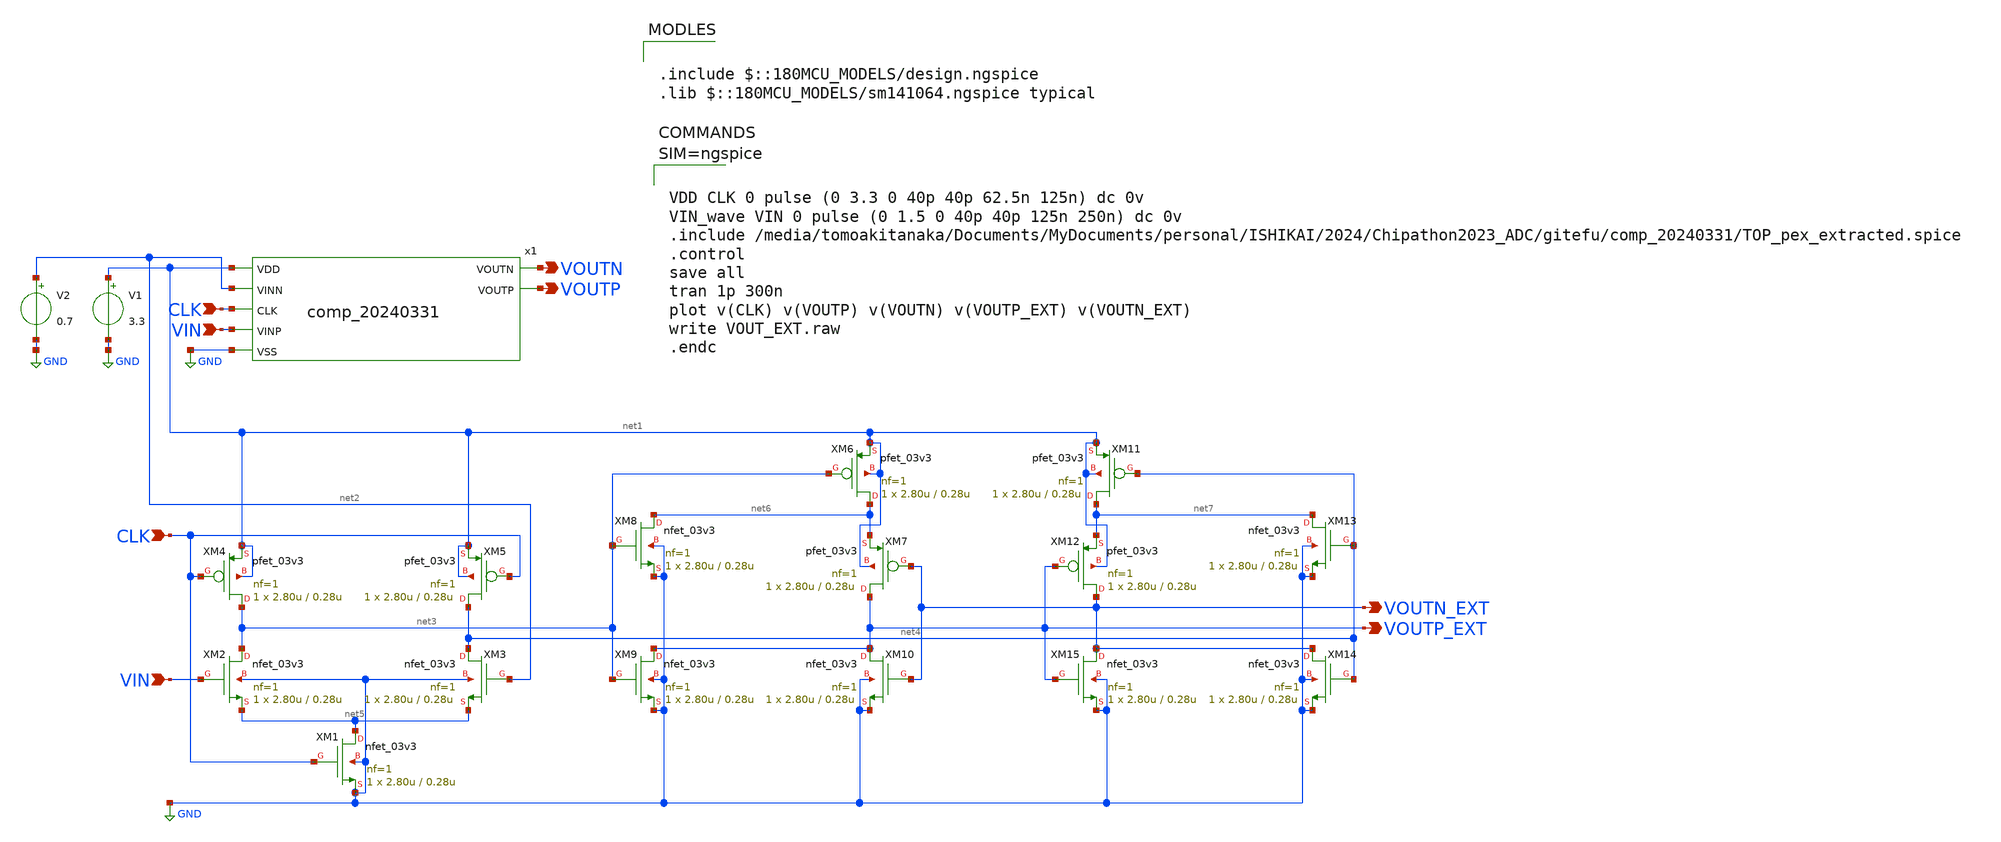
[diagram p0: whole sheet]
** sch_path: gitefu/tb/tb_check_pulse.sch
**.subckt tb_check_pulse CLK VOUTN VOUTP VIN CLK VIN VOUTP_EXT VOUTN_EXT
*.ipin CLK
*.opin VOUTN
*.opin VOUTP
*.ipin VIN
*.ipin CLK
*.ipin VIN
*.opin VOUTP_EXT
*.opin VOUTN_EXT
V1 net1 GND 3.3
V2 net2 GND 0.7
XM1 net5 CLK GND GND nfet_03v3 L=0.28u W=2.80u nf=1 ad='int((nf+1)/2) * W/nf * 0.18u' as='int((nf+2)/2) * W/nf * 0.18u'
+ pd='2*int((nf+1)/2) * (W/nf + 0.18u)' ps='2*int((nf+2)/2) * (W/nf + 0.18u)' nrd='0.18u / W' nrs='0.18u / W'
+ sa=0 sb=0 sd=0 m=1
XM2 net3 VIN net5 GND nfet_03v3 L=0.28u W=2.80u nf=1 ad='int((nf+1)/2) * W/nf * 0.18u' as='int((nf+2)/2) * W/nf * 0.18u'
+ pd='2*int((nf+1)/2) * (W/nf + 0.18u)' ps='2*int((nf+2)/2) * (W/nf + 0.18u)' nrd='0.18u / W' nrs='0.18u / W'
+ sa=0 sb=0 sd=0 m=1
XM4 net3 CLK net1 net1 pfet_03v3 L=0.28u W=2.80u nf=1 ad='int((nf+1)/2) * W/nf * 0.18u' as='int((nf+2)/2) * W/nf * 0.18u'
+ pd='2*int((nf+1)/2) * (W/nf + 0.18u)' ps='2*int((nf+2)/2) * (W/nf + 0.18u)' nrd='0.18u / W' nrs='0.18u / W'
+ sa=0 sb=0 sd=0 m=1
XM6 net6 net3 net1 net1 pfet_03v3 L=0.28u W=2.80u nf=1 ad='int((nf+1)/2) * W/nf * 0.18u' as='int((nf+2)/2) * W/nf * 0.18u'
+ pd='2*int((nf+1)/2) * (W/nf + 0.18u)' ps='2*int((nf+2)/2) * (W/nf + 0.18u)' nrd='0.18u / W' nrs='0.18u / W'
+ sa=0 sb=0 sd=0 m=1
XM7 VOUTP_EXT VOUTN_EXT net6 net1 pfet_03v3 L=0.28u W=2.80u nf=1 ad='int((nf+1)/2) * W/nf * 0.18u' as='int((nf+2)/2) * W/nf * 0.18u'
+ pd='2*int((nf+1)/2) * (W/nf + 0.18u)' ps='2*int((nf+2)/2) * (W/nf + 0.18u)' nrd='0.18u / W' nrs='0.18u / W'
+ sa=0 sb=0 sd=0 m=1
XM8 net6 net3 GND GND nfet_03v3 L=0.28u W=2.80u nf=1 ad='int((nf+1)/2) * W/nf * 0.18u' as='int((nf+2)/2) * W/nf * 0.18u'
+ pd='2*int((nf+1)/2) * (W/nf + 0.18u)' ps='2*int((nf+2)/2) * (W/nf + 0.18u)' nrd='0.18u / W' nrs='0.18u / W'
+ sa=0 sb=0 sd=0 m=1
XM9 VOUTP_EXT net3 GND GND nfet_03v3 L=0.28u W=2.80u nf=1 ad='int((nf+1)/2) * W/nf * 0.18u' as='int((nf+2)/2) * W/nf * 0.18u'
+ pd='2*int((nf+1)/2) * (W/nf + 0.18u)' ps='2*int((nf+2)/2) * (W/nf + 0.18u)' nrd='0.18u / W' nrs='0.18u / W'
+ sa=0 sb=0 sd=0 m=1
XM10 VOUTP_EXT VOUTN_EXT GND GND nfet_03v3 L=0.28u W=2.80u nf=1 ad='int((nf+1)/2) * W/nf * 0.18u' as='int((nf+2)/2) * W/nf * 0.18u'
+ pd='2*int((nf+1)/2) * (W/nf + 0.18u)' ps='2*int((nf+2)/2) * (W/nf + 0.18u)' nrd='0.18u / W' nrs='0.18u / W'
+ sa=0 sb=0 sd=0 m=1
XM3 net4 net2 net5 GND nfet_03v3 L=0.28u W=2.80u nf=1 ad='int((nf+1)/2) * W/nf * 0.18u' as='int((nf+2)/2) * W/nf * 0.18u'
+ pd='2*int((nf+1)/2) * (W/nf + 0.18u)' ps='2*int((nf+2)/2) * (W/nf + 0.18u)' nrd='0.18u / W' nrs='0.18u / W'
+ sa=0 sb=0 sd=0 m=1
XM5 net4 CLK net1 net1 pfet_03v3 L=0.28u W=2.80u nf=1 ad='int((nf+1)/2) * W/nf * 0.18u' as='int((nf+2)/2) * W/nf * 0.18u'
+ pd='2*int((nf+1)/2) * (W/nf + 0.18u)' ps='2*int((nf+2)/2) * (W/nf + 0.18u)' nrd='0.18u / W' nrs='0.18u / W'
+ sa=0 sb=0 sd=0 m=1
XM11 net7 net4 net1 net1 pfet_03v3 L=0.28u W=2.80u nf=1 ad='int((nf+1)/2) * W/nf * 0.18u' as='int((nf+2)/2) * W/nf * 0.18u'
+ pd='2*int((nf+1)/2) * (W/nf + 0.18u)' ps='2*int((nf+2)/2) * (W/nf + 0.18u)' nrd='0.18u / W' nrs='0.18u / W'
+ sa=0 sb=0 sd=0 m=1
XM12 VOUTN_EXT VOUTP_EXT net7 net1 pfet_03v3 L=0.28u W=2.80u nf=1 ad='int((nf+1)/2) * W/nf * 0.18u' as='int((nf+2)/2) * W/nf * 0.18u'
+ pd='2*int((nf+1)/2) * (W/nf + 0.18u)' ps='2*int((nf+2)/2) * (W/nf + 0.18u)' nrd='0.18u / W' nrs='0.18u / W'
+ sa=0 sb=0 sd=0 m=1
XM13 net7 net4 GND GND nfet_03v3 L=0.28u W=2.80u nf=1 ad='int((nf+1)/2) * W/nf * 0.18u' as='int((nf+2)/2) * W/nf * 0.18u'
+ pd='2*int((nf+1)/2) * (W/nf + 0.18u)' ps='2*int((nf+2)/2) * (W/nf + 0.18u)' nrd='0.18u / W' nrs='0.18u / W'
+ sa=0 sb=0 sd=0 m=1
XM14 VOUTN_EXT net4 GND GND nfet_03v3 L=0.28u W=2.80u nf=1 ad='int((nf+1)/2) * W/nf * 0.18u' as='int((nf+2)/2) * W/nf * 0.18u'
+ pd='2*int((nf+1)/2) * (W/nf + 0.18u)' ps='2*int((nf+2)/2) * (W/nf + 0.18u)' nrd='0.18u / W' nrs='0.18u / W'
+ sa=0 sb=0 sd=0 m=1
XM15 VOUTN_EXT VOUTP_EXT GND GND nfet_03v3 L=0.28u W=2.80u nf=1 ad='int((nf+1)/2) * W/nf * 0.18u' as='int((nf+2)/2) * W/nf * 0.18u'
+ pd='2*int((nf+1)/2) * (W/nf + 0.18u)' ps='2*int((nf+2)/2) * (W/nf + 0.18u)' nrd='0.18u / W' nrs='0.18u / W'
+ sa=0 sb=0 sd=0 m=1
x1 net1 CLK VOUTP VOUTN VIN net2 GND TOP
**** begin user architecture code

.include $::180MCU_MODELS/design.ngspice
.lib $::180MCU_MODELS/sm141064.ngspice typical




VDD CLK 0 pulse (0 3.3 0 40p 40p 62.5n 125n) dc 0v
VIN_wave VIN 0 pulse (0 1.5 0 40p 40p 125n 250n) dc 0v
.include /media/tomoakitanaka/Documents/MyDocuments/personal/ISHIKAI/2024/Chipathon2023_ADC/gitefu/comp_20240331/TOP_pex_extracted.spice
.control
save all
tran 1p 300n
plot v(CLK) v(VOUTP) v(VOUTN) v(VOUTP_EXT) v(VOUTN_EXT)
write VOUT_EXT.raw
.endc



**** end user architecture code
**.ends
.GLOBAL GND
.end
